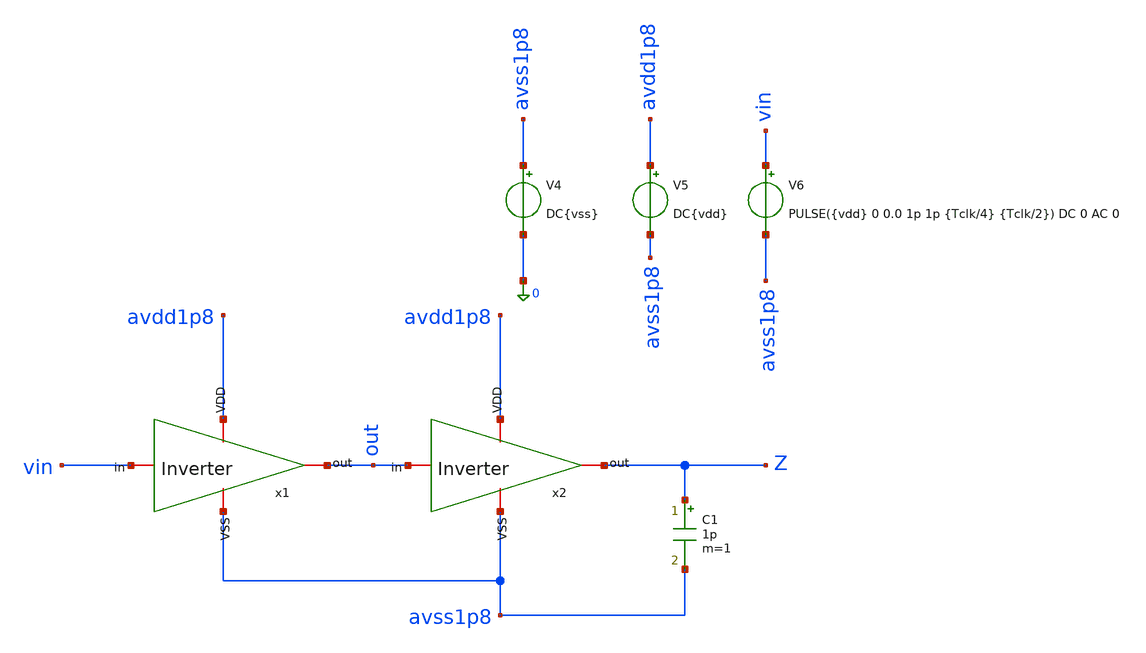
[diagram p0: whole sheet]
** sch_path: verification/testbenches/tb_inverter.sch
**.subckt tb_inverter
x1 avdd1p8 out vin avss1p8 inverter
x2 avdd1p8 Z out avss1p8 inverter
V5 avdd1p8 avss1p8 DC{vdd}
V4 avss1p8 0 DC{vss}
V6 vin avss1p8 PULSE({vdd} 0 0.0 1p 1p {Tclk/4} {Tclk/2}) DC 0 AC 0
C1 Z avss1p8 1p m=1
**** begin user architecture code


* Circuit Parameters
.param vdd = 1.2
.param vss = 0.0
.param Tclk = 10n
.options TEMP = 27.0
* Include Models - IHP SG13G2
.lib cornerMOSlv.lib mos_tt
* OP Parameters & Singals to save
.save all
*Simulations
.control
tran 0.01u 10n
setplot tran1
plot v(vin) v(out)+1.2
reset
dc V6 0 1.2 0.01
setplot dc
plot vin vout ylabel vout xlabel vin
set filetype = ascii
write dcsweep.raw
.endc
.end


**** end user architecture code
**.ends

* expanding   symbol:  blocks/inverter/schematic/inverter.sym # of pins=4
** sym_path: design/blocks/inverter/schematic/inverter.sym
** sch_path: design/blocks/inverter/schematic/inverter.sch
.subckt inverter VDD out in VSS
*.iopin VDD
*.iopin in
*.iopin out
*.iopin VSS
XM3 out in VDD VDD sg13_lv_pmos w=1.5u l=0.15u ng=1 m=1 mm_ok=1
XM4 out in VSS VSS sg13_lv_nmos w=0.75u l=0.15u ng=1 m=1 mm_ok=1
.ends

.end
